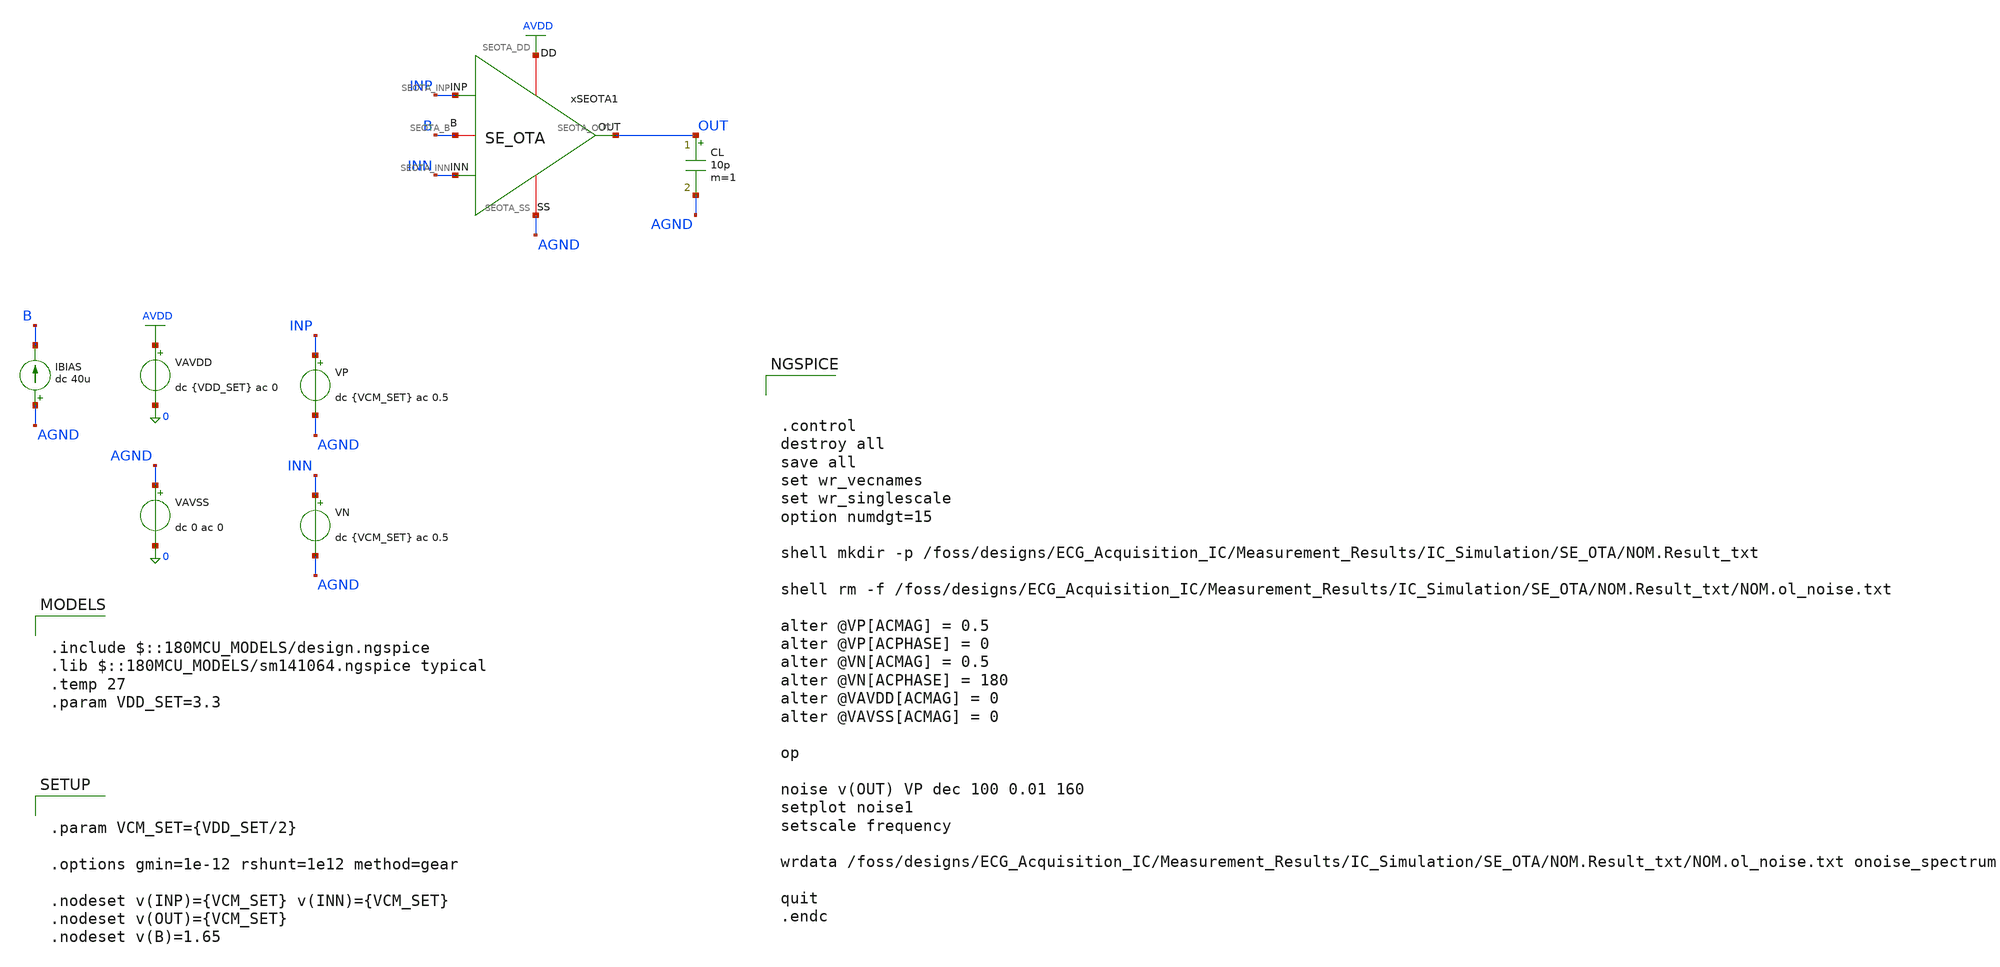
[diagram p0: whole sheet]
** sch_path: Design_Files/IC Design/Testbench/SE_OTA/Open_Loop_Noise/SE_OTA_TB_OL_NOISE_NOM.sch
**.subckt SE_OTA_TB_OL_NOISE_NOM
IBIAS AGND B dc 40u
VAVDD AVDD 0 dc {VDD_SET} ac 0
.save i(vavdd)
CL OUT AGND 10p m=1
xSEOTA1 AVDD AGND INP INN OUT B SE_OTA
VAVSS AGND 0 dc 0 ac 0
.save i(vavss)
VP INP AGND dc {VCM_SET} ac 0.5
VN INN AGND dc {VCM_SET} ac 0.5
**** begin user architecture code

.include $::180MCU_MODELS/design.ngspice
.lib $::180MCU_MODELS/sm141064.ngspice typical
.temp 27
.param VDD_SET=3.3



.param VCM_SET={VDD_SET/2}

.options gmin=1e-12 rshunt=1e12 method=gear

.nodeset v(INP)={VCM_SET} v(INN)={VCM_SET}
.nodeset v(OUT)={VCM_SET}
.nodeset v(B)=1.65





.control
destroy all
save all
set wr_vecnames
set wr_singlescale
option numdgt=15

shell mkdir -p
+ /foss/designs/ECG_Acquisition_IC/Measurement_Results/IC_Simulation/SE_OTA/NOM.Result_txt

shell rm -f
+ /foss/designs/ECG_Acquisition_IC/Measurement_Results/IC_Simulation/SE_OTA/NOM.Result_txt/NOM.ol_noise.txt

alter @VP[ACMAG] = 0.5
alter @VP[ACPHASE] = 0
alter @VN[ACMAG] = 0.5
alter @VN[ACPHASE] = 180
alter @VAVDD[ACMAG] = 0
alter @VAVSS[ACMAG] = 0

op

noise v(OUT) VP dec 100 0.01 160
setplot noise1
setscale frequency

wrdata
+ /foss/designs/ECG_Acquisition_IC/Measurement_Results/IC_Simulation/SE_OTA/NOM.Result_txt/NOM.ol_noise.txt onoise_spectrum

quit
.endc


**** end user architecture code
**.ends

* expanding   symbol:  ECG_Acquisition_IC/Design_Files/IC Design/Schematic/SE_OTA/SE_OTA.sym # of
*+ pins=6
** sym_path: Design_Files/IC Design/Schematic/SE_OTA/SE_OTA.sym
** sch_path: Design_Files/IC Design/Schematic/SE_OTA/SE_OTA.sch
.subckt SE_OTA SEOTA_DD SEOTA_SS SEOTA_INP SEOTA_INN SEOTA_OUT SEOTA_B
*.iopin SEOTA_DD
*.iopin SEOTA_SS
*.ipin SEOTA_INP
*.ipin SEOTA_INN
*.opin SEOTA_OUT
*.iopin SEOTA_B
XM3 net4 net4 SEOTA_DD SEOTA_DD pfet_03v3 L=4u W=1u nf=1 ad='int((nf+1)/2) * W/nf * 0.18u' as='int((nf+2)/2) * W/nf * 0.18u'
+ pd='2*int((nf+1)/2) * (W/nf + 0.18u)' ps='2*int((nf+2)/2) * (W/nf + 0.18u)' nrd='0.18u / W' nrs='0.18u / W'
+ sa=0 sb=0 sd=0 m=60
XM7 SEOTA_OUT SEOTA_B SEOTA_SS SEOTA_SS nfet_03v3 L=0.5u W=1u nf=1 ad='int((nf+1)/2) * W/nf * 0.18u'
+ as='int((nf+2)/2) * W/nf * 0.18u' pd='2*int((nf+1)/2) * (W/nf + 0.18u)' ps='2*int((nf+2)/2) * (W/nf + 0.18u)'
+ nrd='0.18u / W' nrs='0.18u / W' sa=0 sb=0 sd=0 m=100
Rz net1 net2 3.8k m=1
XM5 net3 SEOTA_B SEOTA_SS SEOTA_SS nfet_03v3 L=2u W=1u nf=1 ad='int((nf+1)/2) * W/nf * 0.18u' as='int((nf+2)/2) * W/nf * 0.18u'
+ pd='2*int((nf+1)/2) * (W/nf + 0.18u)' ps='2*int((nf+2)/2) * (W/nf + 0.18u)' nrd='0.18u / W' nrs='0.18u / W'
+ sa=0 sb=0 sd=0 m=10
XM6 SEOTA_OUT net1 SEOTA_DD SEOTA_DD pfet_03v3 L=0.5u W=1u nf=1 ad='int((nf+1)/2) * W/nf * 0.18u' as='int((nf+2)/2) * W/nf * 0.18u'
+ pd='2*int((nf+1)/2) * (W/nf + 0.18u)' ps='2*int((nf+2)/2) * (W/nf + 0.18u)' nrd='0.18u / W' nrs='0.18u / W'
+ sa=0 sb=0 sd=0 m=400
XM8 SEOTA_B SEOTA_B SEOTA_SS SEOTA_SS nfet_03v3 L=2u W=1u nf=1 ad='int((nf+1)/2) * W/nf * 0.18u' as='int((nf+2)/2) * W/nf * 0.18u'
+ pd='2*int((nf+1)/2) * (W/nf + 0.18u)' ps='2*int((nf+2)/2) * (W/nf + 0.18u)' nrd='0.18u / W' nrs='0.18u / W'
+ sa=0 sb=0 sd=0 m=20
Cc net2 SEOTA_OUT 2p m=1
XM4 net1 net4 SEOTA_DD SEOTA_DD pfet_03v3 L=4u W=1u nf=1 ad='int((nf+1)/2) * W/nf * 0.18u' as='int((nf+2)/2) * W/nf * 0.18u'
+ pd='2*int((nf+1)/2) * (W/nf + 0.18u)' ps='2*int((nf+2)/2) * (W/nf + 0.18u)' nrd='0.18u / W' nrs='0.18u / W'
+ sa=0 sb=0 sd=0 m=60
XM1 net4 SEOTA_INN net3 SEOTA_SS nfet_03v3 L=4u W=1u nf=1 ad='int((nf+1)/2) * W/nf * 0.18u' as='int((nf+2)/2) * W/nf * 0.18u'
+ pd='2*int((nf+1)/2) * (W/nf + 0.18u)' ps='2*int((nf+2)/2) * (W/nf + 0.18u)' nrd='0.18u / W' nrs='0.18u / W'
+ sa=0 sb=0 sd=0 m=400
XM2 net1 SEOTA_INP net3 SEOTA_SS nfet_03v3 L=4u W=1u nf=1 ad='int((nf+1)/2) * W/nf * 0.18u' as='int((nf+2)/2) * W/nf * 0.18u'
+ pd='2*int((nf+1)/2) * (W/nf + 0.18u)' ps='2*int((nf+2)/2) * (W/nf + 0.18u)' nrd='0.18u / W' nrs='0.18u / W'
+ sa=0 sb=0 sd=0 m=400
.ends

.GLOBAL AVDD
.end
